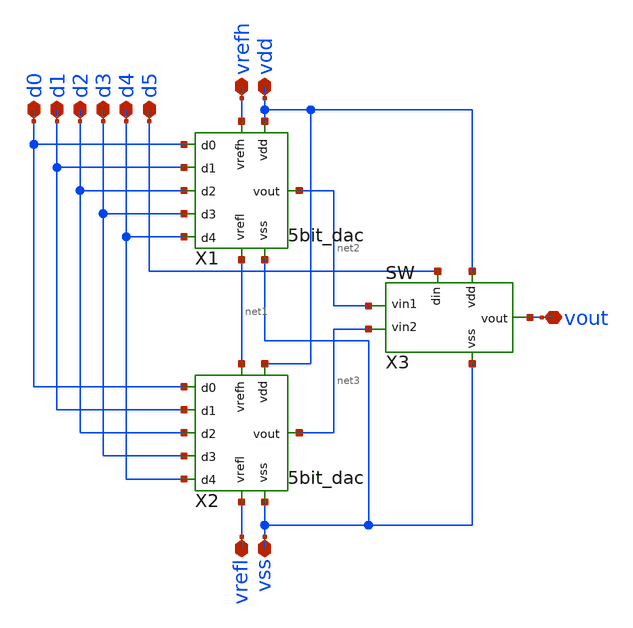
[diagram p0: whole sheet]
** sch_path: dac5v/1.schematics/6bit_dac.sch
**.subckt 6bit_dac vdd vss vrefh vrefl d0 d1 d2 d3 d4 d5 vout
*.iopin vdd
*.iopin vss
*.iopin vrefh
*.iopin vrefl
*.iopin d0
*.iopin d1
*.iopin d2
*.iopin d3
*.iopin d4
*.iopin d5
*.iopin vout
X1 vdd vrefh vss net1 d0 d1 d2 d3 d4 net2 5bit_dac
X2 vdd net1 vss vrefl d0 d1 d2 d3 d4 net3 5bit_dac
X3 vdd vss d5 net2 net3 vout sw
**.ends

* expanding   symbol:  /home/97ms/uci/ip/dac5v/1.schematics/5bit_dac.sym # of pins=10
** sym_path: dac5v/1.schematics/5bit_dac.sym
** sch_path: dac5v/1.schematics/5bit_dac.sch
.subckt 5bit_dac vdd vrefh vss vrefl d0 d1 d2 d3 d4 vout
*.iopin vdd
*.iopin vss
*.iopin vrefh
*.iopin vrefl
*.iopin d0
*.iopin d1
*.iopin d2
*.iopin d3
*.iopin d4
*.iopin vout
X1 vdd vss vrefh net1 d0 d1 d2 d3 net2 4bit_dac
X2 vdd vss net1 vrefl d0 d1 d2 d3 net3 4bit_dac
X3 vdd vss d4 net2 net3 vout sw
.ends


* expanding   symbol:  /home/97ms/uci/ip/dac5v/1.schematics/sw.sym # of pins=6
** sym_path: dac5v/1.schematics/sw.sym
** sch_path: dac5v/1.schematics/sw.sch
.subckt sw vdd vss din vin1 vin2 vout
*.iopin vdd
*.iopin vss
*.iopin din
*.iopin vin1
*.iopin vin2
*.iopin vout
XM2 net2 net1 vdd vdd sky130_fd_pr__pfet_g5v0d10v5 L=0.5 W=1 nf=1 ad='int((nf+1)/2) * W/nf * 0.29' as='int((nf+2)/2) * W/nf * 0.29'
+ pd='2*int((nf+1)/2) * (W/nf + 0.29)' ps='2*int((nf+2)/2) * (W/nf + 0.29)' nrd='0.29 / W' nrs='0.29 / W'
+ sa=0 sb=0 sd=0 mult=1 m=1
XM1 net1 din vdd vdd sky130_fd_pr__pfet_g5v0d10v5 L=0.5 W=1 nf=1 ad='int((nf+1)/2) * W/nf * 0.29' as='int((nf+2)/2) * W/nf * 0.29'
+ pd='2*int((nf+1)/2) * (W/nf + 0.29)' ps='2*int((nf+2)/2) * (W/nf + 0.29)' nrd='0.29 / W' nrs='0.29 / W'
+ sa=0 sb=0 sd=0 mult=1 m=1
XM3 vout net1 vin1 vdd sky130_fd_pr__pfet_g5v0d10v5 L=0.5 W=1 nf=1 ad='int((nf+1)/2) * W/nf * 0.29' as='int((nf+2)/2) * W/nf * 0.29'
+ pd='2*int((nf+1)/2) * (W/nf + 0.29)' ps='2*int((nf+2)/2) * (W/nf + 0.29)' nrd='0.29 / W' nrs='0.29 / W'
+ sa=0 sb=0 sd=0 mult=1 m=1
XM4 vin2 net2 vout vdd sky130_fd_pr__pfet_g5v0d10v5 L=0.5 W=1 nf=1 ad='int((nf+1)/2) * W/nf * 0.29' as='int((nf+2)/2) * W/nf * 0.29'
+ pd='2*int((nf+1)/2) * (W/nf + 0.29)' ps='2*int((nf+2)/2) * (W/nf + 0.29)' nrd='0.29 / W' nrs='0.29 / W'
+ sa=0 sb=0 sd=0 mult=1 m=1
XM5 net1 din vss vss sky130_fd_pr__nfet_g5v0d10v5 L=0.5 W=0.42 nf=1 ad='int((nf+1)/2) * W/nf * 0.29'
+ as='int((nf+2)/2) * W/nf * 0.29' pd='2*int((nf+1)/2) * (W/nf + 0.29)' ps='2*int((nf+2)/2) * (W/nf + 0.29)'
+ nrd='0.29 / W' nrs='0.29 / W' sa=0 sb=0 sd=0 mult=1 m=1
XM6 net2 net1 vss vss sky130_fd_pr__nfet_g5v0d10v5 L=0.5 W=0.42 nf=1 ad='int((nf+1)/2) * W/nf * 0.29'
+ as='int((nf+2)/2) * W/nf * 0.29' pd='2*int((nf+1)/2) * (W/nf + 0.29)' ps='2*int((nf+2)/2) * (W/nf + 0.29)'
+ nrd='0.29 / W' nrs='0.29 / W' sa=0 sb=0 sd=0 mult=1 m=1
XM7 vout net1 vin2 vss sky130_fd_pr__nfet_g5v0d10v5 L=0.5 W=0.42 nf=1 ad='int((nf+1)/2) * W/nf * 0.29'
+ as='int((nf+2)/2) * W/nf * 0.29' pd='2*int((nf+1)/2) * (W/nf + 0.29)' ps='2*int((nf+2)/2) * (W/nf + 0.29)'
+ nrd='0.29 / W' nrs='0.29 / W' sa=0 sb=0 sd=0 mult=1 m=1
XM8 vin1 net2 vout vss sky130_fd_pr__nfet_g5v0d10v5 L=0.5 W=0.42 nf=1 ad='int((nf+1)/2) * W/nf * 0.29'
+ as='int((nf+2)/2) * W/nf * 0.29' pd='2*int((nf+1)/2) * (W/nf + 0.29)' ps='2*int((nf+2)/2) * (W/nf + 0.29)'
+ nrd='0.29 / W' nrs='0.29 / W' sa=0 sb=0 sd=0 mult=1 m=1
.ends


* expanding   symbol:  /home/97ms/uci/ip/dac5v/1.schematics/4bit_dac.sym # of pins=9
** sym_path: dac5v/1.schematics/4bit_dac.sym
** sch_path: dac5v/1.schematics/4bit_dac.sch
.subckt 4bit_dac vdd vss vrefh vrefl d0 d1 d2 d3 vout
*.iopin vdd
*.iopin vss
*.iopin vrefh
*.iopin vrefl
*.iopin d0
*.iopin d1
*.iopin d2
*.iopin d3
*.iopin vout
X1 vdd vss vrefh net2 d0 d1 d2 net1 3bit_dac
X2 vdd vss net2 vrefl d0 d1 d2 net3 3bit_dac
X3 vdd vss d3 net1 net3 vout sw
.ends


* expanding   symbol:  /home/97ms/uci/ip/dac5v/1.schematics/3bit_dac.sym # of pins=8
** sym_path: dac/1.schematics/3bit_dac.sym
** sch_path: dac/1.schematics/3bit_dac.sch
.subckt 3bit_dac vdd vss vrefh vrefl d0 d1 d2 vout
*.iopin vdd
*.iopin vss
*.iopin vrefh
*.iopin vrefl
*.iopin d0
*.iopin d1
*.iopin d2
*.iopin vout
X1 vdd vss vrefh net3 d0 d1 net1 2bit_dac
X2 vdd vss net3 vrefl d0 d1 net2 2bit_dac
X3 vdd vss d2 net1 net2 vout sw
.ends


* expanding   symbol:  /home/97ms/uci/ip/dac/1.schematics/2bit_dac.sym # of pins=7
** sym_path: dac/1.schematics/2bit_dac.sym
** sch_path: dac/1.schematics/2bit_dac.sch
.subckt 2bit_dac vdd vss vrefh vrefl d0 d1 vout
*.iopin vdd
*.iopin vss
*.iopin vrefh
*.iopin vrefl
*.iopin d0
*.iopin d1
*.iopin vout
X1 vdd vss d0 net3 net4 net2 sw
X2 vdd vss d0 net5 vrefl net1 sw
X3 vdd vss d1 net2 net1 vout sw
XR1 net3 vrefh vss sky130_fd_pr__res_high_po_0p35 L=1.09 mult=1 m=1
XR2 net4 net3 vss sky130_fd_pr__res_high_po_0p35 L=1.09 mult=1 m=1
XR3 net5 net4 vss sky130_fd_pr__res_high_po_0p35 L=1.09 mult=1 m=1
XR4 vrefl net5 vss sky130_fd_pr__res_high_po_0p35 L=1.09 mult=1 m=1
.ends

.end
